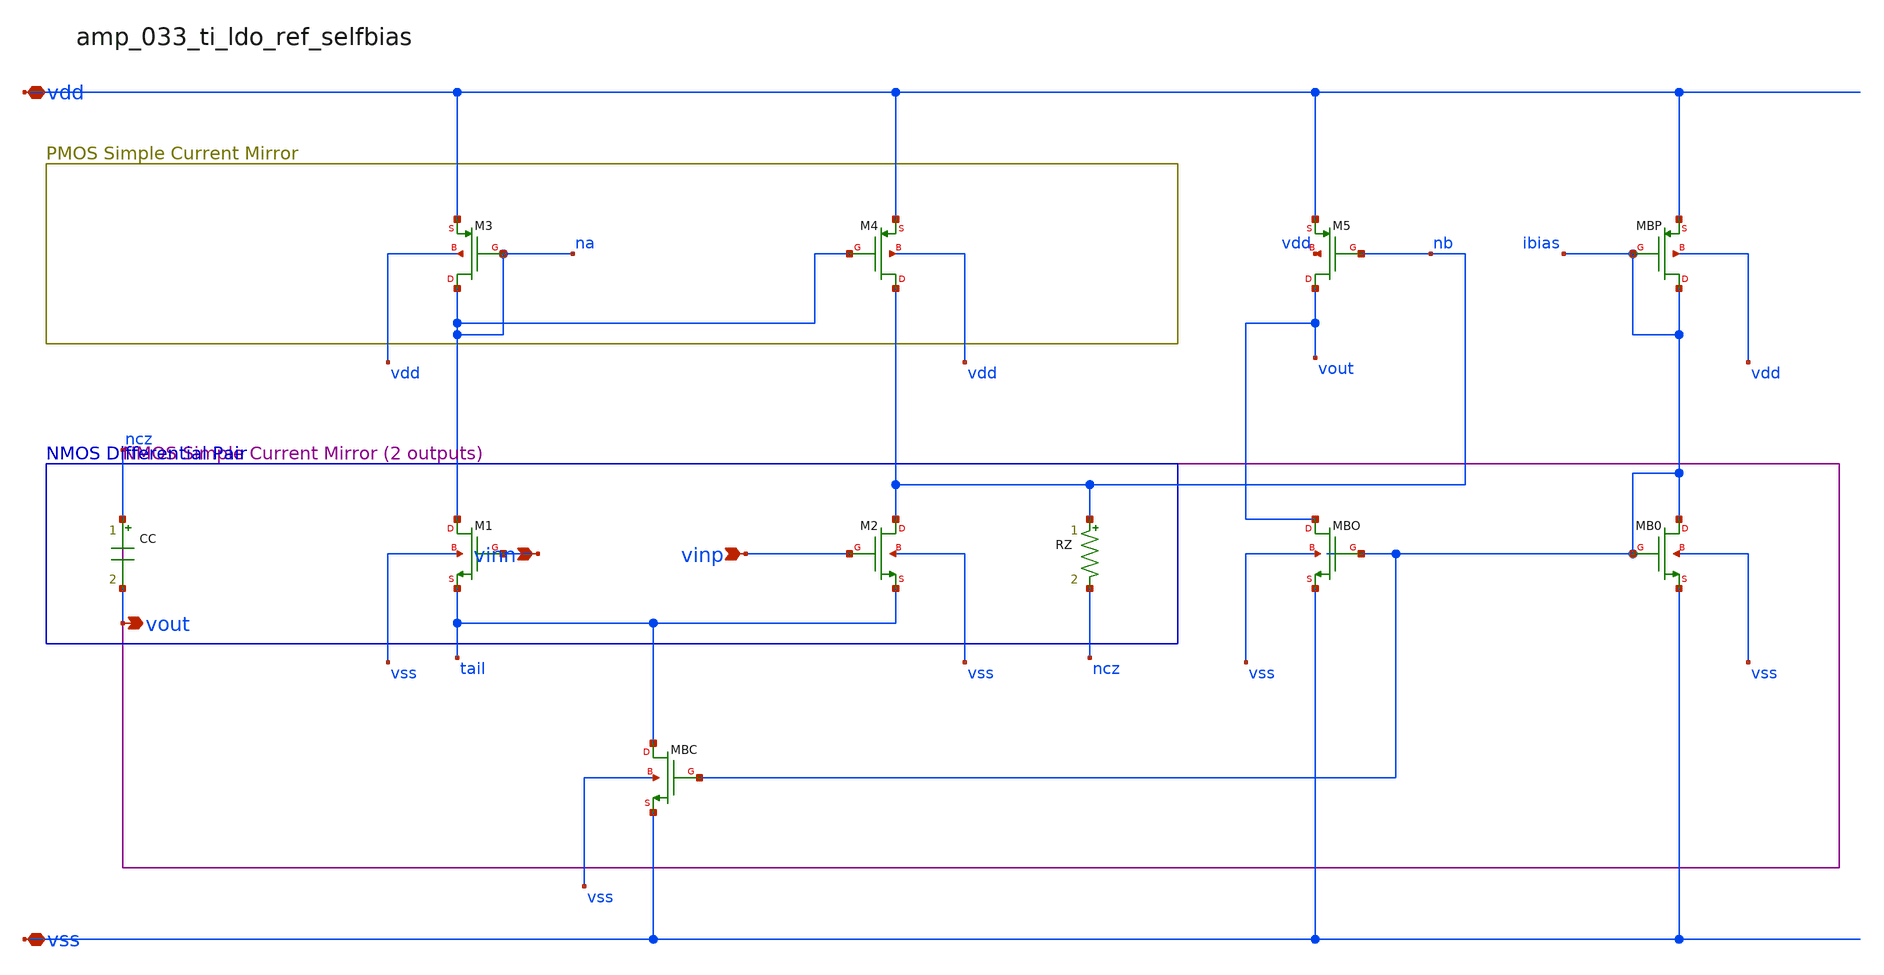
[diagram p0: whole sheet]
** sch_path: analog-db/raw/amp_033_ti_ldo_ref_selfbias/amp_033_ti_ldo_ref_selfbias_annotated.sch
**.subckt amp_033_ti_ldo_ref_selfbias_annotated vinn vinp vdd vss vout
*.ipin vinn
*.ipin vinp
*.iopin vdd
*.iopin vss
*.opin vout
CC ncz vout 'c_comp' m=1
RZ nb ncz 'r_z' m=1
XM1 na vinn tail vss sg13_lv_nmos w=x_dut_xm1_w l=x_dut_xm1_l ng=1 m=1
XM2 nb vinp tail vss sg13_lv_nmos w=x_dut_xm2_w l=x_dut_xm2_l ng=1 m=1
XM3 na na vdd vdd sg13_lv_pmos w=x_dut_xm3_w l=x_dut_xm3_l ng=1 m=1
XM4 nb na vdd vdd sg13_lv_pmos w=x_dut_xm4_w l=x_dut_xm4_l ng=1 m=1
XM5 vout nb vdd vdd sg13_lv_pmos w=x_dut_xm5_w l=x_dut_xm5_l ng=1 m=1
XMB0 ibias ibias vss vss sg13_lv_nmos w=x_dut_xmb0_w l=x_dut_xmb0_l ng=1 m=1
XMBC tail ibias vss vss sg13_lv_nmos w=x_dut_xmbc_w l=x_dut_xmbc_l ng=1 m=x_dut_xmbc_m
XMBO vout ibias vss vss sg13_lv_nmos w=x_dut_xmbo_w l=x_dut_xmbo_l ng=1 m=x_dut_xmbo_m
XMBP ibias ibias vdd vdd sg13_lv_pmos w=x_dut_xmbp_w l=x_dut_xmbp_l ng=1 m=1
**.ends
.end
